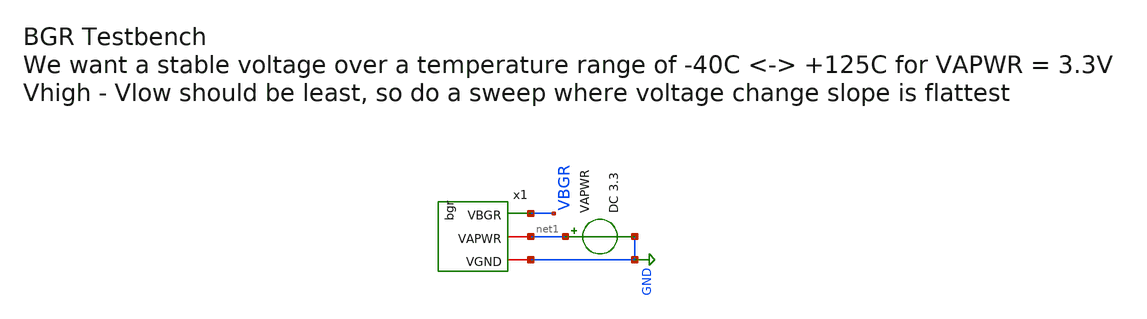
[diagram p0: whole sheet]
** sch_path: xschem/tb_bgr.sch
**.subckt tb_bgr
VAPWR net1 GND DC 3.3
x1 VBGR net1 GND bgr
**** begin user architecture code





**** end user architecture code
**.ends

* expanding   symbol:  bgr.sym # of pins=3
** sym_path: xschem/bgr.sym
** sch_path: xschem/bgr.sch
.subckt bgr VBGR VAPWR VGND
*.iopin VAPWR
*.iopin VGND
*.opin VBGR
.ends

.GLOBAL GND
.end
